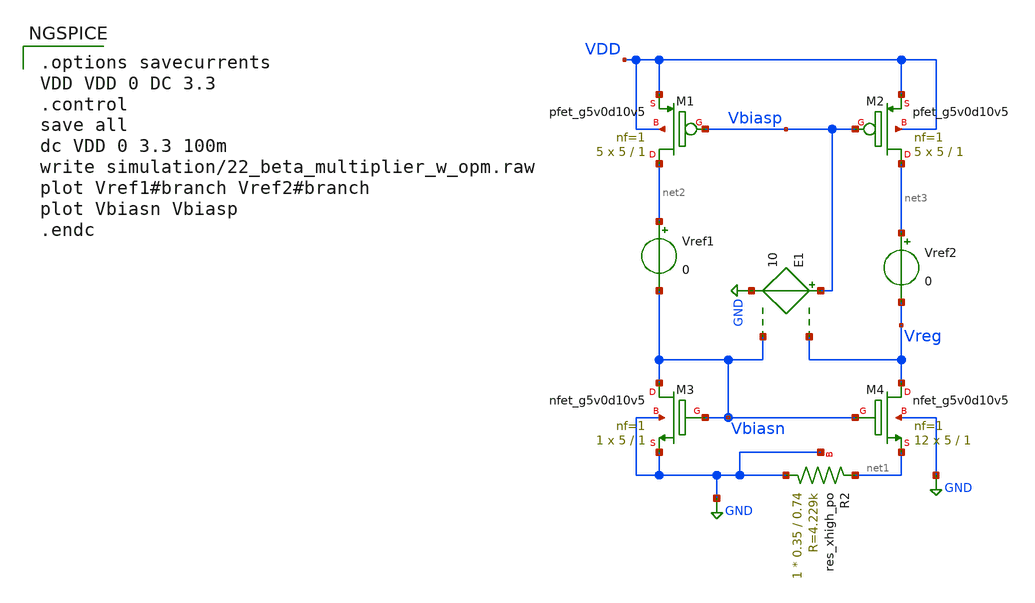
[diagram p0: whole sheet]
** sch_path: xschem/22_beta_multiplier_w_opm.sch
**.subckt 22_beta_multiplier_w_opm
XM1 net2 Vbiasp VDD VDD sky130_fd_pr__pfet_g5v0d10v5 L=1 W=5 nf=1 ad='int((nf+1)/2) * W/nf * 0.29' as='int((nf+2)/2) * W/nf * 0.29'
+ pd='2*int((nf+1)/2) * (W/nf + 0.29)' ps='2*int((nf+2)/2) * (W/nf + 0.29)' nrd='0.29 / W' nrs='0.29 / W'
+ sa=0 sb=0 sd=0 mult=5 m=5
XM3 Vbiasn Vbiasn GND GND sky130_fd_pr__nfet_g5v0d10v5 L=1 W=5 nf=1 ad='int((nf+1)/2) * W/nf * 0.29'
+ as='int((nf+2)/2) * W/nf * 0.29' pd='2*int((nf+1)/2) * (W/nf + 0.29)' ps='2*int((nf+2)/2) * (W/nf + 0.29)'
+ nrd='0.29 / W' nrs='0.29 / W' sa=0 sb=0 sd=0 mult=1 m=1
XM2 net3 Vbiasp VDD VDD sky130_fd_pr__pfet_g5v0d10v5 L=1 W=5 nf=1 ad='int((nf+1)/2) * W/nf * 0.29' as='int((nf+2)/2) * W/nf * 0.29'
+ pd='2*int((nf+1)/2) * (W/nf + 0.29)' ps='2*int((nf+2)/2) * (W/nf + 0.29)' nrd='0.29 / W' nrs='0.29 / W'
+ sa=0 sb=0 sd=0 mult=5 m=5
XM4 Vreg Vbiasn net1 GND sky130_fd_pr__nfet_g5v0d10v5 L=1 W=5 nf=1 ad='int((nf+1)/2) * W/nf * 0.29' as='int((nf+2)/2) * W/nf * 0.29'
+ pd='2*int((nf+1)/2) * (W/nf + 0.29)' ps='2*int((nf+2)/2) * (W/nf + 0.29)' nrd='0.29 / W' nrs='0.29 / W'
+ sa=0 sb=0 sd=0 mult=12 m=12
Vref1 net2 Vbiasn 0
Vref2 net3 Vreg 0
XR2 GND net1 GND sky130_fd_pr__res_xhigh_po W=0.35 L=0.74 mult=1 m=1
E1 Vbiasp GND Vreg Vbiasn 10
**** begin user architecture code

.options savecurrents
VDD VDD 0 DC 3.3
.control
save all
dc VDD 0 3.3 100m
write simulation/22_beta_multiplier_w_opm.raw
plot Vref1#branch Vref2#branch
plot Vbiasn Vbiasp
.endc



** opencircuitdesign pdks install
.lib $::SKYWATER_MODELS/sky130.lib.spice tt


**** end user architecture code
**.ends
.GLOBAL GND
.end
